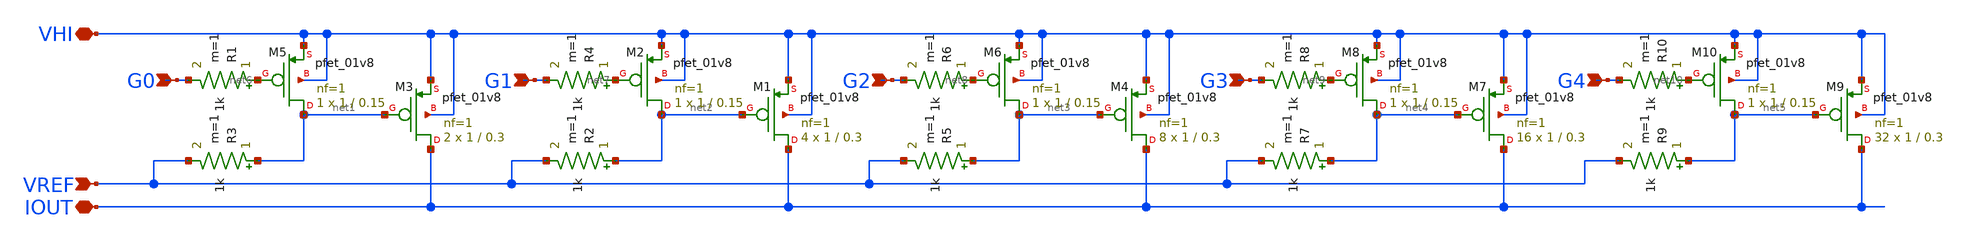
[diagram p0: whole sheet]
** sch_path: xschem/pmirror_tunable_64x.sch
**.subckt pmirror_tunable_64x G0 G1 G2 G3 G4 VREF VHI IOUT
*.ipin G0
*.ipin G1
*.ipin G2
*.ipin G3
*.ipin G4
*.ipin VREF
*.iopin VHI
*.iopin IOUT
XM3 IOUT net1 VHI VHI sky130_fd_pr__pfet_01v8 L=0.3 W=1 nf=1 ad='int((nf+1)/2) * W/nf * 0.29' as='int((nf+2)/2) * W/nf * 0.29'
+ pd='2*int((nf+1)/2) * (W/nf + 0.29)' ps='2*int((nf+2)/2) * (W/nf + 0.29)' nrd='0.29 / W' nrs='0.29 / W'
+ sa=0 sb=0 sd=0 mult=2 m=2
XM5 net1 net6 VHI VHI sky130_fd_pr__pfet_01v8 L=0.15 W=1 nf=1 ad='int((nf+1)/2) * W/nf * 0.29' as='int((nf+2)/2) * W/nf * 0.29'
+ pd='2*int((nf+1)/2) * (W/nf + 0.29)' ps='2*int((nf+2)/2) * (W/nf + 0.29)' nrd='0.29 / W' nrs='0.29 / W'
+ sa=0 sb=0 sd=0 mult=1 m=1
R3 net1 VREF 1k m=1
R1 net6 G0 1k m=1
XM1 IOUT net2 VHI VHI sky130_fd_pr__pfet_01v8 L=0.3 W=1 nf=1 ad='int((nf+1)/2) * W/nf * 0.29' as='int((nf+2)/2) * W/nf * 0.29'
+ pd='2*int((nf+1)/2) * (W/nf + 0.29)' ps='2*int((nf+2)/2) * (W/nf + 0.29)' nrd='0.29 / W' nrs='0.29 / W'
+ sa=0 sb=0 sd=0 mult=4 m=4
XM2 net2 net7 VHI VHI sky130_fd_pr__pfet_01v8 L=0.15 W=1 nf=1 ad='int((nf+1)/2) * W/nf * 0.29' as='int((nf+2)/2) * W/nf * 0.29'
+ pd='2*int((nf+1)/2) * (W/nf + 0.29)' ps='2*int((nf+2)/2) * (W/nf + 0.29)' nrd='0.29 / W' nrs='0.29 / W'
+ sa=0 sb=0 sd=0 mult=1 m=1
R2 net2 VREF 1k m=1
R4 net7 G1 1k m=1
XM4 IOUT net3 VHI VHI sky130_fd_pr__pfet_01v8 L=0.3 W=1 nf=1 ad='int((nf+1)/2) * W/nf * 0.29' as='int((nf+2)/2) * W/nf * 0.29'
+ pd='2*int((nf+1)/2) * (W/nf + 0.29)' ps='2*int((nf+2)/2) * (W/nf + 0.29)' nrd='0.29 / W' nrs='0.29 / W'
+ sa=0 sb=0 sd=0 mult=8 m=8
XM6 net3 net8 VHI VHI sky130_fd_pr__pfet_01v8 L=0.15 W=1 nf=1 ad='int((nf+1)/2) * W/nf * 0.29' as='int((nf+2)/2) * W/nf * 0.29'
+ pd='2*int((nf+1)/2) * (W/nf + 0.29)' ps='2*int((nf+2)/2) * (W/nf + 0.29)' nrd='0.29 / W' nrs='0.29 / W'
+ sa=0 sb=0 sd=0 mult=1 m=1
R5 net3 VREF 1k m=1
R6 net8 G2 1k m=1
XM7 IOUT net4 VHI VHI sky130_fd_pr__pfet_01v8 L=0.3 W=1 nf=1 ad='int((nf+1)/2) * W/nf * 0.29' as='int((nf+2)/2) * W/nf * 0.29'
+ pd='2*int((nf+1)/2) * (W/nf + 0.29)' ps='2*int((nf+2)/2) * (W/nf + 0.29)' nrd='0.29 / W' nrs='0.29 / W'
+ sa=0 sb=0 sd=0 mult=16 m=16
XM8 net4 net9 VHI VHI sky130_fd_pr__pfet_01v8 L=0.15 W=1 nf=1 ad='int((nf+1)/2) * W/nf * 0.29' as='int((nf+2)/2) * W/nf * 0.29'
+ pd='2*int((nf+1)/2) * (W/nf + 0.29)' ps='2*int((nf+2)/2) * (W/nf + 0.29)' nrd='0.29 / W' nrs='0.29 / W'
+ sa=0 sb=0 sd=0 mult=1 m=1
R7 net4 VREF 1k m=1
R8 net9 G3 1k m=1
XM9 IOUT net5 VHI VHI sky130_fd_pr__pfet_01v8 L=0.3 W=1 nf=1 ad='int((nf+1)/2) * W/nf * 0.29' as='int((nf+2)/2) * W/nf * 0.29'
+ pd='2*int((nf+1)/2) * (W/nf + 0.29)' ps='2*int((nf+2)/2) * (W/nf + 0.29)' nrd='0.29 / W' nrs='0.29 / W'
+ sa=0 sb=0 sd=0 mult=32 m=32
XM10 net5 net10 VHI VHI sky130_fd_pr__pfet_01v8 L=0.15 W=1 nf=1 ad='int((nf+1)/2) * W/nf * 0.29' as='int((nf+2)/2) * W/nf * 0.29'
+ pd='2*int((nf+1)/2) * (W/nf + 0.29)' ps='2*int((nf+2)/2) * (W/nf + 0.29)' nrd='0.29 / W' nrs='0.29 / W'
+ sa=0 sb=0 sd=0 mult=1 m=1
R9 net5 VREF 1k m=1
R10 net10 G4 1k m=1
**.ends
.end
